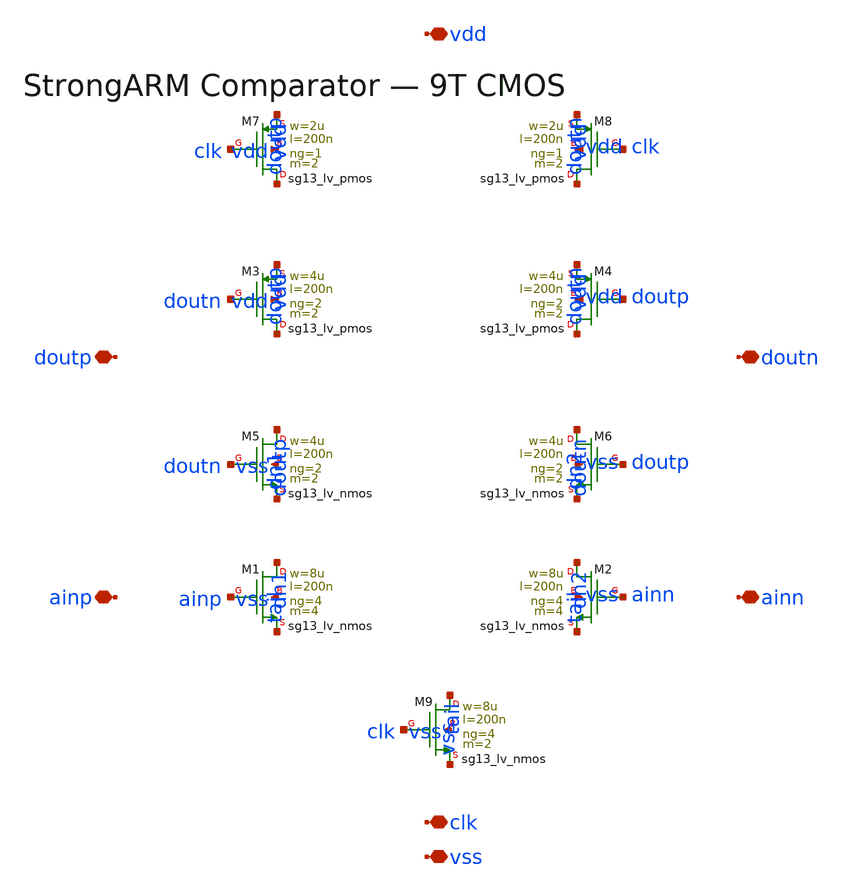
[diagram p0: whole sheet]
** sch_path: xschem/blocks/ADC_SAR_12B.sch
**.subckt ADC_SAR_12B ainp ainn clk doutp doutn vdd vss
*.iopin ainp
*.iopin ainn
*.iopin clk
*.iopin doutp
*.iopin doutn
*.iopin vdd
*.iopin vss
XM1 dn1 ainp tail vss sg13_lv_nmos w=8u l=200n ng=4 m=4 mm_ok=1
XM2 dn2 ainn tail vss sg13_lv_nmos w=8u l=200n ng=4 m=4 mm_ok=1
XM9 tail clk vss vss sg13_lv_nmos w=8u l=200n ng=4 m=2 mm_ok=1
XM5 doutp doutn dn1 vss sg13_lv_nmos w=4u l=200n ng=2 m=2 mm_ok=1
XM6 doutn doutp dn2 vss sg13_lv_nmos w=4u l=200n ng=2 m=2 mm_ok=1
XM3 doutp doutn vdd vdd sg13_lv_pmos w=4u l=200n ng=2 m=2 mm_ok=1
XM4 doutn doutp vdd vdd sg13_lv_pmos w=4u l=200n ng=2 m=2 mm_ok=1
XM7 doutp clk vdd vdd sg13_lv_pmos w=2u l=200n ng=1 m=2 mm_ok=1
XM8 doutn clk vdd vdd sg13_lv_pmos w=2u l=200n ng=1 m=2 mm_ok=1
**.ends
.end
